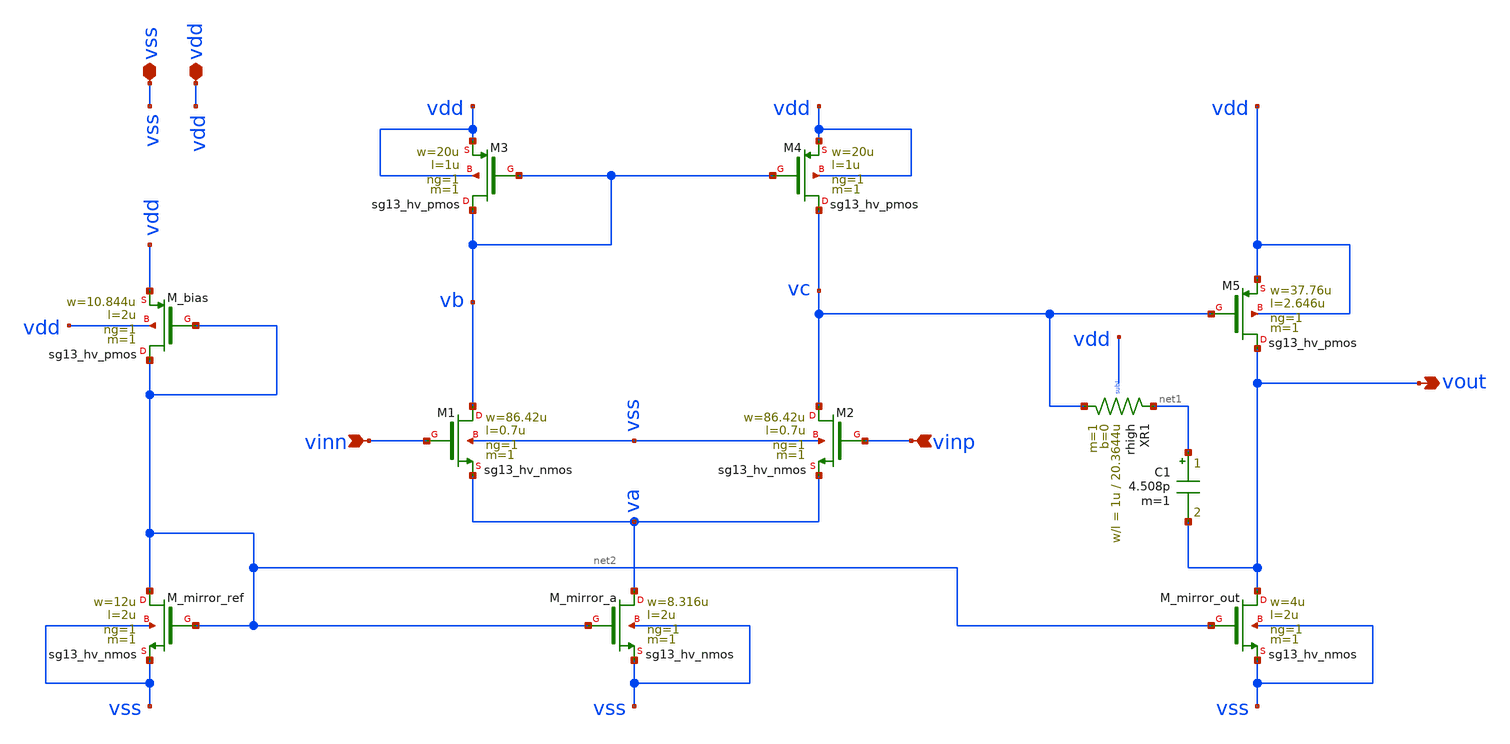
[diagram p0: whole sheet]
** sch_path: analog-db/drawings/ldo-005-ti-ldo-buffer-ref/ihp130/ref_amp/ref_amp.sch
**.subckt ref_amp vinn vinp vdd vss vout
*.ipin vinn
*.ipin vinp
*.iopin vdd
*.iopin vss
*.opin vout
XM1 vb vinn va vss sg13_hv_nmos w=86.42u l=0.7u ng=1 m=1 mm_ok=1
XM2 vc vinp va vss sg13_hv_nmos w=86.42u l=0.7u ng=1 m=1 mm_ok=1
XM3 vb vb vdd vdd sg13_hv_pmos w=20u l=1u ng=1 m=1 mm_ok=1
XM4 vc vb vdd vdd sg13_hv_pmos w=20u l=1u ng=1 m=1 mm_ok=1
XM5 vout vc vdd vdd sg13_hv_pmos w=37.76u l=2.646u ng=1 m=1 mm_ok=1
C1 net1 vout 4.508p m=1
XR1 vc net1 sub! rhigh w=1u l=20.3644u m=1 b=0
XM_mirror_a va net2 vss vss sg13_hv_nmos w=8.316u l=2u ng=1 m=1 mm_ok=1
XM_mirror_out vout net2 vss vss sg13_hv_nmos w=4u l=2u ng=1 m=1 mm_ok=1
XM_mirror_ref net2 net2 vss vss sg13_hv_nmos w=12u l=2u ng=1 m=1 mm_ok=1
XM_bias net2 net2 vdd vdd sg13_hv_pmos w=10.844u l=2u ng=1 m=1 mm_ok=1
**.ends
.end
